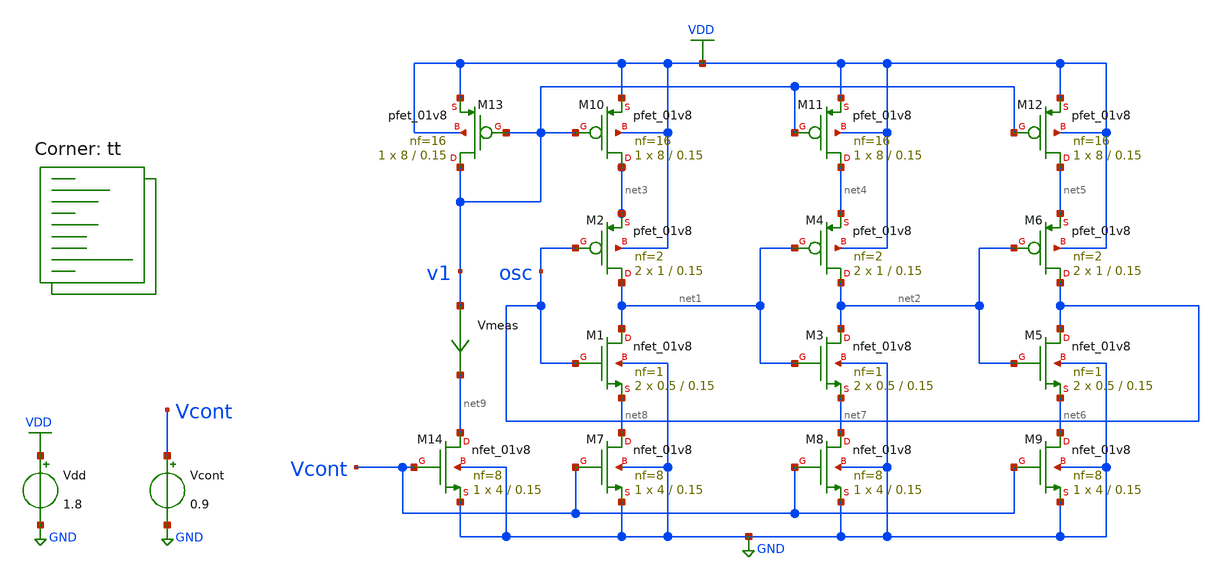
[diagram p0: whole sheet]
** sch_path: projects/pll/vco/xschem_ngspice/tb_current_starved_VCO.sch
**.subckt tb_current_starved_VCO
XM1 net1 osc net8 GND sky130_fd_pr__nfet_01v8 L=0.15 W=0.5 nf=1 ad='int((nf+1)/2) * W/nf * 0.29' as='int((nf+2)/2) * W/nf * 0.29'
+ pd='2*int((nf+1)/2) * (W/nf + 0.29)' ps='2*int((nf+2)/2) * (W/nf + 0.29)' nrd='0.29 / W' nrs='0.29 / W'
+ sa=0 sb=0 sd=0 mult=2 m=2
XM2 net1 osc net3 VDD sky130_fd_pr__pfet_01v8 L=0.15 W=1 nf=2 ad='int((nf+1)/2) * W/nf * 0.29' as='int((nf+2)/2) * W/nf * 0.29'
+ pd='2*int((nf+1)/2) * (W/nf + 0.29)' ps='2*int((nf+2)/2) * (W/nf + 0.29)' nrd='0.29 / W' nrs='0.29 / W'
+ sa=0 sb=0 sd=0 mult=2 m=2
XM3 net2 net1 net7 GND sky130_fd_pr__nfet_01v8 L=0.15 W=0.5 nf=1 ad='int((nf+1)/2) * W/nf * 0.29' as='int((nf+2)/2) * W/nf * 0.29'
+ pd='2*int((nf+1)/2) * (W/nf + 0.29)' ps='2*int((nf+2)/2) * (W/nf + 0.29)' nrd='0.29 / W' nrs='0.29 / W'
+ sa=0 sb=0 sd=0 mult=2 m=2
XM4 net2 net1 net4 VDD sky130_fd_pr__pfet_01v8 L=0.15 W=1 nf=2 ad='int((nf+1)/2) * W/nf * 0.29' as='int((nf+2)/2) * W/nf * 0.29'
+ pd='2*int((nf+1)/2) * (W/nf + 0.29)' ps='2*int((nf+2)/2) * (W/nf + 0.29)' nrd='0.29 / W' nrs='0.29 / W'
+ sa=0 sb=0 sd=0 mult=2 m=2
XM5 osc net2 net6 GND sky130_fd_pr__nfet_01v8 L=0.15 W=0.5 nf=1 ad='int((nf+1)/2) * W/nf * 0.29' as='int((nf+2)/2) * W/nf * 0.29'
+ pd='2*int((nf+1)/2) * (W/nf + 0.29)' ps='2*int((nf+2)/2) * (W/nf + 0.29)' nrd='0.29 / W' nrs='0.29 / W'
+ sa=0 sb=0 sd=0 mult=2 m=2
XM6 osc net2 net5 VDD sky130_fd_pr__pfet_01v8 L=0.15 W=1 nf=2 ad='int((nf+1)/2) * W/nf * 0.29' as='int((nf+2)/2) * W/nf * 0.29'
+ pd='2*int((nf+1)/2) * (W/nf + 0.29)' ps='2*int((nf+2)/2) * (W/nf + 0.29)' nrd='0.29 / W' nrs='0.29 / W'
+ sa=0 sb=0 sd=0 mult=2 m=2
XM7 net8 Vcont GND GND sky130_fd_pr__nfet_01v8 L=0.15 W=4 nf=8 ad='int((nf+1)/2) * W/nf * 0.29' as='int((nf+2)/2) * W/nf * 0.29'
+ pd='2*int((nf+1)/2) * (W/nf + 0.29)' ps='2*int((nf+2)/2) * (W/nf + 0.29)' nrd='0.29 / W' nrs='0.29 / W'
+ sa=0 sb=0 sd=0 mult=1 m=1
XM8 net7 Vcont GND GND sky130_fd_pr__nfet_01v8 L=0.15 W=4 nf=8 ad='int((nf+1)/2) * W/nf * 0.29' as='int((nf+2)/2) * W/nf * 0.29'
+ pd='2*int((nf+1)/2) * (W/nf + 0.29)' ps='2*int((nf+2)/2) * (W/nf + 0.29)' nrd='0.29 / W' nrs='0.29 / W'
+ sa=0 sb=0 sd=0 mult=1 m=1
XM9 net6 Vcont GND GND sky130_fd_pr__nfet_01v8 L=0.15 W=4 nf=8 ad='int((nf+1)/2) * W/nf * 0.29' as='int((nf+2)/2) * W/nf * 0.29'
+ pd='2*int((nf+1)/2) * (W/nf + 0.29)' ps='2*int((nf+2)/2) * (W/nf + 0.29)' nrd='0.29 / W' nrs='0.29 / W'
+ sa=0 sb=0 sd=0 mult=1 m=1
XM10 net3 v1 VDD VDD sky130_fd_pr__pfet_01v8 L=0.15 W=8 nf=16 ad='int((nf+1)/2) * W/nf * 0.29' as='int((nf+2)/2) * W/nf * 0.29'
+ pd='2*int((nf+1)/2) * (W/nf + 0.29)' ps='2*int((nf+2)/2) * (W/nf + 0.29)' nrd='0.29 / W' nrs='0.29 / W'
+ sa=0 sb=0 sd=0 mult=1 m=1
XM11 net4 v1 VDD VDD sky130_fd_pr__pfet_01v8 L=0.15 W=8 nf=16 ad='int((nf+1)/2) * W/nf * 0.29' as='int((nf+2)/2) * W/nf * 0.29'
+ pd='2*int((nf+1)/2) * (W/nf + 0.29)' ps='2*int((nf+2)/2) * (W/nf + 0.29)' nrd='0.29 / W' nrs='0.29 / W'
+ sa=0 sb=0 sd=0 mult=1 m=1
XM12 net5 v1 VDD VDD sky130_fd_pr__pfet_01v8 L=0.15 W=8 nf=16 ad='int((nf+1)/2) * W/nf * 0.29' as='int((nf+2)/2) * W/nf * 0.29'
+ pd='2*int((nf+1)/2) * (W/nf + 0.29)' ps='2*int((nf+2)/2) * (W/nf + 0.29)' nrd='0.29 / W' nrs='0.29 / W'
+ sa=0 sb=0 sd=0 mult=1 m=1
Vdd VDD GND 1.8
Vcont Vcont GND 0.9
XM13 v1 v1 VDD VDD sky130_fd_pr__pfet_01v8 L=0.15 W=8 nf=16 ad='int((nf+1)/2) * W/nf * 0.29' as='int((nf+2)/2) * W/nf * 0.29'
+ pd='2*int((nf+1)/2) * (W/nf + 0.29)' ps='2*int((nf+2)/2) * (W/nf + 0.29)' nrd='0.29 / W' nrs='0.29 / W'
+ sa=0 sb=0 sd=0 mult=1 m=1
XM14 net9 Vcont GND GND sky130_fd_pr__nfet_01v8 L=0.15 W=4 nf=8 ad='int((nf+1)/2) * W/nf * 0.29' as='int((nf+2)/2) * W/nf * 0.29'
+ pd='2*int((nf+1)/2) * (W/nf + 0.29)' ps='2*int((nf+2)/2) * (W/nf + 0.29)' nrd='0.29 / W' nrs='0.29 / W'
+ sa=0 sb=0 sd=0 mult=1 m=1
Vmeas v1 net9 0
.save i(vmeas)
**** begin user architecture code
.lib $::SKYWATER_MODELS/sky130.lib.spice tt



.option method=gear
.option wnflag=1


*.ic v(osc)=0

*.temp = 75

.control
  let v_cont_start = 0.0
  let v_cont_stop = 1.9

  dowhile v_cont_start <= v_cont_stop
    alter vcont $&v_cont_start
    save v(osc) v(vcont) v(v1)
    tran 0.5ps 30ns
    remzerovec
    write tb_current_starved_VCO_{$&v_cont_start}.raw
    * write tb_current_starved_VCO.raw
    let filename = v_cont_start * 100
    wrdata /foss/designs/my_design/projects/pll/vco/xschem_ngspice/tb_current_starved_VCO_{$&filename}.txt
+ v(osc)
    set appendwrite

    reset
    let v_cont_start = v_cont_start + 0.1
  end
.endc






**** end user architecture code
**.ends
.GLOBAL VDD
.GLOBAL GND
.end
